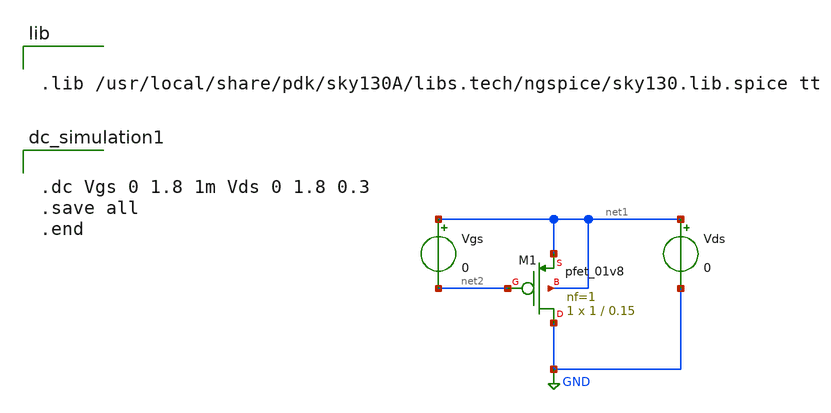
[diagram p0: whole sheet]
** sch_path: xschem/pmos.sch
**.subckt pmos
Vgs net1 net2 0
Vds net1 GND 0
XM1 GND net2 net1 net1 sky130_fd_pr__pfet_01v8 L=0.15 W=1 nf=1 ad='int((nf+1)/2) * W/nf * 0.29' as='int((nf+2)/2) * W/nf * 0.29'
+ pd='2*int((nf+1)/2) * (W/nf + 0.29)' ps='2*int((nf+2)/2) * (W/nf + 0.29)' nrd='0.29 / W' nrs='0.29 / W'
+ sa=0 sb=0 sd=0 mult=1 m=1
**** begin user architecture code


.lib /usr/local/share/pdk/sky130A/libs.tech/ngspice/sky130.lib.spice tt




.dc Vgs 0 1.8 1m Vds 0 1.8 0.3
.save all
.end


**** end user architecture code
**.ends
.GLOBAL GND
.end
